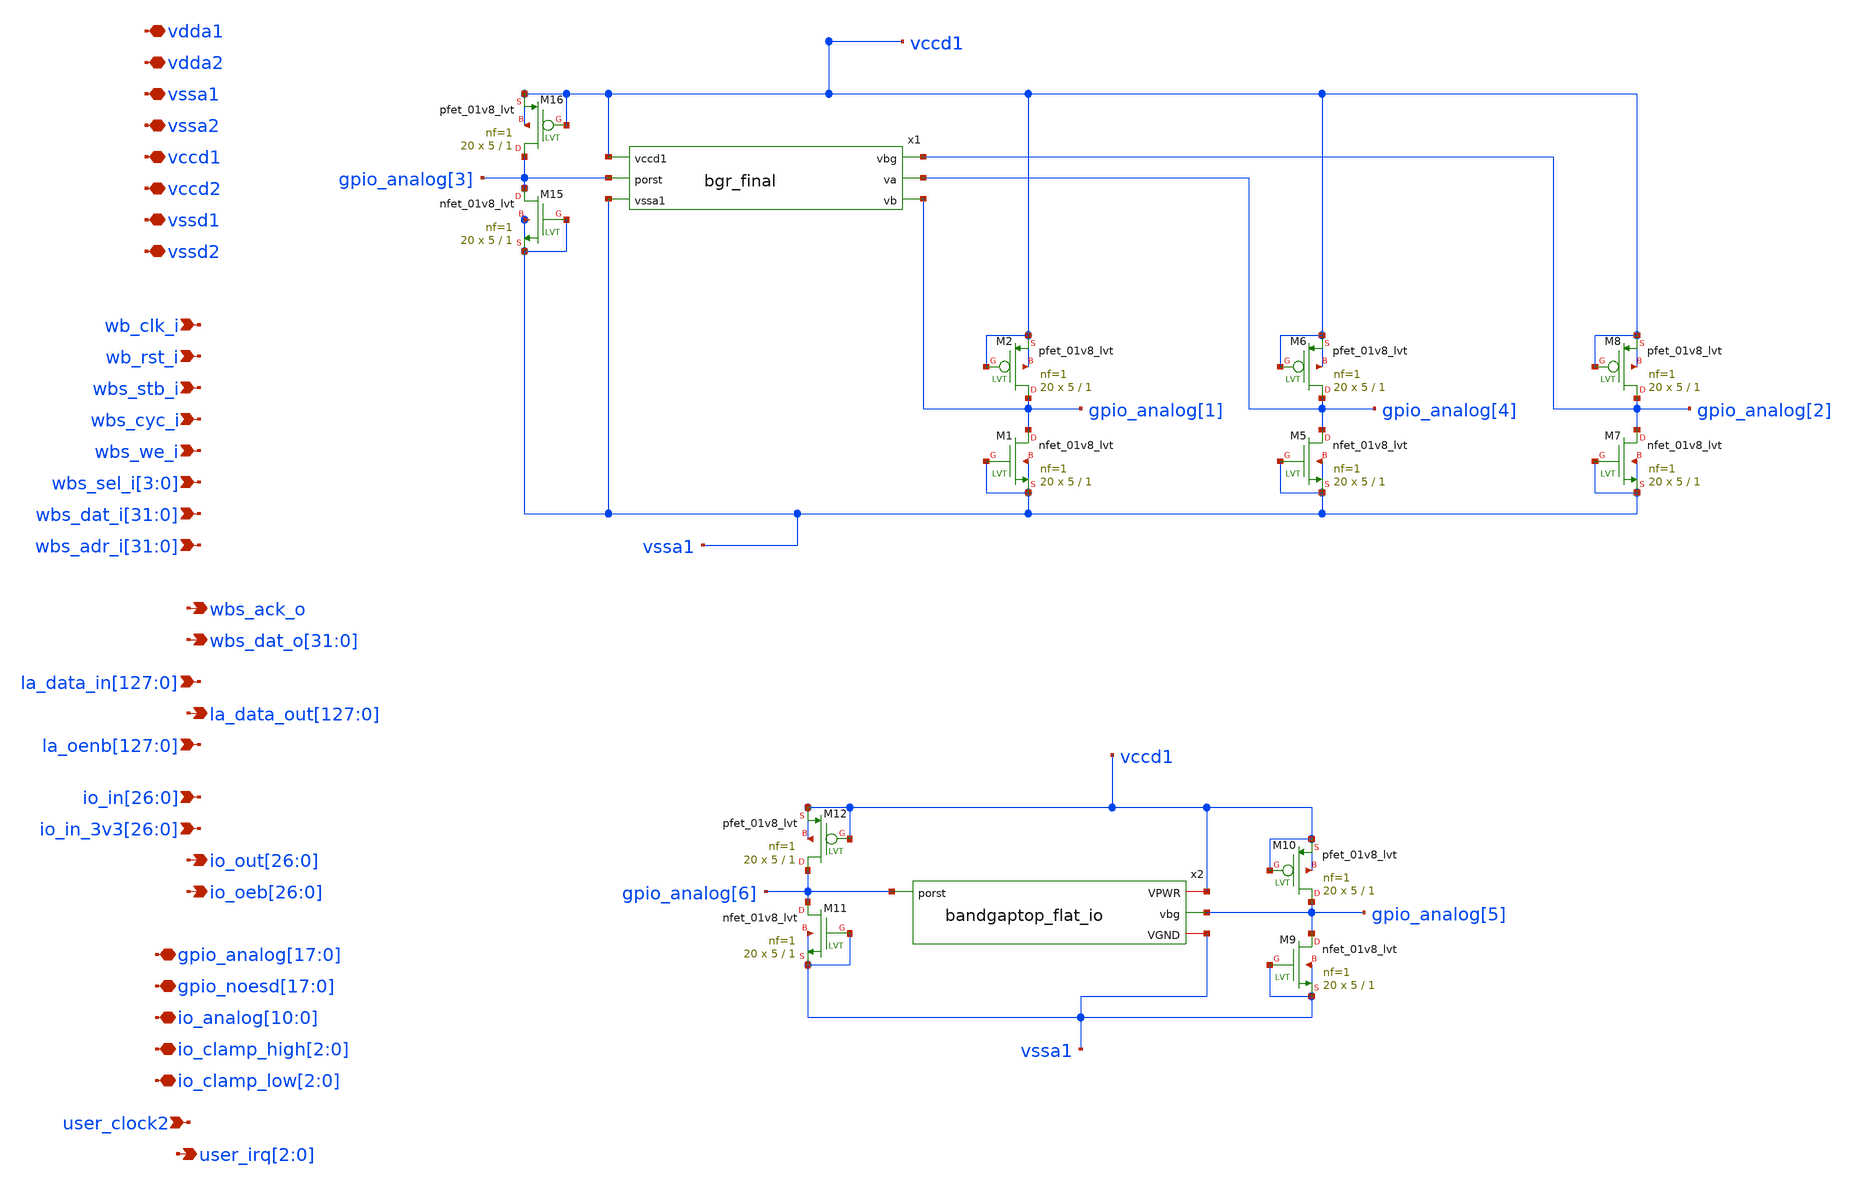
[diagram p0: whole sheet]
** sch_path: xschem/xschem/user_analog_project_wrapper_0.sch
**.subckt user_analog_project_wrapper_0 vdda1 vdda2 vssa1 vssa2 vccd1 vccd2 vssd1 vssd2 wb_clk_i
*+ wb_rst_i wbs_stb_i wbs_cyc_i wbs_we_i wbs_sel_i[3],wbs_sel_i[2],wbs_sel_i[1],wbs_sel_i[0]
*+ wbs_dat_i[31],wbs_dat_i[30],wbs_dat_i[29],wbs_dat_i[28],wbs_dat_i[27],wbs_dat_i[26],wbs_dat_i[25],wbs_dat_i[24],wbs_dat_i[23],wbs_dat_i[22],wbs_dat_i[21],wbs_dat_i[20],wbs_dat_i[19],wbs_dat_i[18],wbs_dat_i[17],wbs_dat_i[16],wbs_dat_i[15],wbs_dat_i[14],wbs_dat_i[13],wbs_dat_i[12],wbs_dat_i[11],wbs_dat_i[10],wbs_dat_i[9],wbs_dat_i[8],wbs_dat_i[7],wbs_dat_i[6],wbs_dat_i[5],wbs_dat_i[4],wbs_dat_i[3],wbs_dat_i[2],wbs_dat_i[1],wbs_dat_i[0]
*+ wbs_adr_i[31],wbs_adr_i[30],wbs_adr_i[29],wbs_adr_i[28],wbs_adr_i[27],wbs_adr_i[26],wbs_adr_i[25],wbs_adr_i[24],wbs_adr_i[23],wbs_adr_i[22],wbs_adr_i[21],wbs_adr_i[20],wbs_adr_i[19],wbs_adr_i[18],wbs_adr_i[17],wbs_adr_i[16],wbs_adr_i[15],wbs_adr_i[14],wbs_adr_i[13],wbs_adr_i[12],wbs_adr_i[11],wbs_adr_i[10],wbs_adr_i[9],wbs_adr_i[8],wbs_adr_i[7],wbs_adr_i[6],wbs_adr_i[5],wbs_adr_i[4],wbs_adr_i[3],wbs_adr_i[2],wbs_adr_i[1],wbs_adr_i[0] wbs_ack_o
*+ wbs_dat_o[31],wbs_dat_o[30],wbs_dat_o[29],wbs_dat_o[28],wbs_dat_o[27],wbs_dat_o[26],wbs_dat_o[25],wbs_dat_o[24],wbs_dat_o[23],wbs_dat_o[22],wbs_dat_o[21],wbs_dat_o[20],wbs_dat_o[19],wbs_dat_o[18],wbs_dat_o[17],wbs_dat_o[16],wbs_dat_o[15],wbs_dat_o[14],wbs_dat_o[13],wbs_dat_o[12],wbs_dat_o[11],wbs_dat_o[10],wbs_dat_o[9],wbs_dat_o[8],wbs_dat_o[7],wbs_dat_o[6],wbs_dat_o[5],wbs_dat_o[4],wbs_dat_o[3],wbs_dat_o[2],wbs_dat_o[1],wbs_dat_o[0]
*+ la_data_in[127],la_data_in[126],la_data_in[125],la_data_in[124],la_data_in[123],la_data_in[122],la_data_in[121],la_data_in[120],la_data_in[119],la_data_in[118],la_data_in[117],la_data_in[116],la_data_in[115],la_data_in[114],la_data_in[113],la_data_in[112],la_data_in[111],la_data_in[110],la_data_in[109],la_data_in[108],la_data_in[107],la_data_in[106],la_data_in[105],la_data_in[104],la_data_in[103],la_data_in[102],la_data_in[101],la_data_in[100],la_data_in[99],la_data_in[98],la_data_in[97],la_data_in[96],la_data_in[95],la_data_in[94],la_data_in[93],la_data_in[92],la_data_in[91],la_data_in[90],la_data_in[89],la_data_in[88],la_data_in[87],la_data_in[86],la_data_in[85],la_data_in[84],la_data_in[83],la_data_in[82],la_data_in[81],la_data_in[80],la_data_in[79],la_data_in[78],la_data_in[77],la_data_in[76],la_data_in[75],la_data_in[74],la_data_in[73],la_data_in[72],la_data_in[71],la_data_in[70],la_data_in[69],la_data_in[68],la_data_in[67],la_data_in[66],la_data_in[65],la_data_in[64],la_data_in[63],la_data_in[62],la_data_in[61],la_data_in[60],la_data_in[59],la_data_in[58],la_data_in[57],la_data_in[56],la_data_in[55],la_data_in[54],la_data_in[53],la_data_in[52],la_data_in[51],la_data_in[50],la_data_in[49],la_data_in[48],la_data_in[47],la_data_in[46],la_data_in[45],la_data_in[44],la_data_in[43],la_data_in[42],la_data_in[41],la_data_in[40],la_data_in[39],la_data_in[38],la_data_in[37],la_data_in[36],la_data_in[35],la_data_in[34],la_data_in[33],la_data_in[32],la_data_in[31],la_data_in[30],la_data_in[29],la_data_in[28],la_data_in[27],la_data_in[26],la_data_in[25],la_data_in[24],la_data_in[23],la_data_in[22],la_data_in[21],la_data_in[20],la_data_in[19],la_data_in[18],la_data_in[17],la_data_in[16],la_data_in[15],la_data_in[14],la_data_in[13],la_data_in[12],la_data_in[11],la_data_in[10],la_data_in[9],la_data_in[8],la_data_in[7],la_data_in[6],la_data_in[5],la_data_in[4],la_data_in[3],la_data_in[2],la_data_in[1],la_data_in[0]
*+ la_data_out[127],la_data_out[126],la_data_out[125],la_data_out[124],la_data_out[123],la_data_out[122],la_data_out[121],la_data_out[120],la_data_out[119],la_data_out[118],la_data_out[117],la_data_out[116],la_data_out[115],la_data_out[114],la_data_out[113],la_data_out[112],la_data_out[111],la_data_out[110],la_data_out[109],la_data_out[108],la_data_out[107],la_data_out[106],la_data_out[105],la_data_out[104],la_data_out[103],la_data_out[102],la_data_out[101],la_data_out[100],la_data_out[99],la_data_out[98],la_data_out[97],la_data_out[96],la_data_out[95],la_data_out[94],la_data_out[93],la_data_out[92],la_data_out[91],la_data_out[90],la_data_out[89],la_data_out[88],la_data_out[87],la_data_out[86],la_data_out[85],la_data_out[84],la_data_out[83],la_data_out[82],la_data_out[81],la_data_out[80],la_data_out[79],la_data_out[78],la_data_out[77],la_data_out[76],la_data_out[75],la_data_out[74],la_data_out[73],la_data_out[72],la_data_out[71],la_data_out[70],la_data_out[69],la_data_out[68],la_data_out[67],la_data_out[66],la_data_out[65],la_data_out[64],la_data_out[63],la_data_out[62],la_data_out[61],la_data_out[60],la_data_out[59],la_data_out[58],la_data_out[57],la_data_out[56],la_data_out[55],la_data_out[54],la_data_out[53],la_data_out[52],la_data_out[51],la_data_out[50],la_data_out[49],la_data_out[48],la_data_out[47],la_data_out[46],la_data_out[45],la_data_out[44],la_data_out[43],la_data_out[42],la_data_out[41],la_data_out[40],la_data_out[39],la_data_out[38],la_data_out[37],la_data_out[36],la_data_out[35],la_data_out[34],la_data_out[33],la_data_out[32],la_data_out[31],la_data_out[30],la_data_out[29],la_data_out[28],la_data_out[27],la_data_out[26],la_data_out[25],la_data_out[24],la_data_out[23],la_data_out[22],la_data_out[21],la_data_out[20],la_data_out[19],la_data_out[18],la_data_out[17],la_data_out[16],la_data_out[15],la_data_out[14],la_data_out[13],la_data_out[12],la_data_out[11],la_data_out[10],la_data_out[9],la_data_out[8],la_data_out[7],la_data_out[6],la_data_out[5],la_data_out[4],la_data_out[3],la_data_out[2],la_data_out[1],la_data_out[0]
*+ io_in[26],io_in[25],io_in[24],io_in[23],io_in[22],io_in[21],io_in[20],io_in[19],io_in[18],io_in[17],io_in[16],io_in[15],io_in[14],io_in[13],io_in[12],io_in[11],io_in[10],io_in[9],io_in[8],io_in[7],io_in[6],io_in[5],io_in[4],io_in[3],io_in[2],io_in[1],io_in[0]
*+ io_in_3v3[26],io_in_3v3[25],io_in_3v3[24],io_in_3v3[23],io_in_3v3[22],io_in_3v3[21],io_in_3v3[20],io_in_3v3[19],io_in_3v3[18],io_in_3v3[17],io_in_3v3[16],io_in_3v3[15],io_in_3v3[14],io_in_3v3[13],io_in_3v3[12],io_in_3v3[11],io_in_3v3[10],io_in_3v3[9],io_in_3v3[8],io_in_3v3[7],io_in_3v3[6],io_in_3v3[5],io_in_3v3[4],io_in_3v3[3],io_in_3v3[2],io_in_3v3[1],io_in_3v3[0] user_clock2
*+ io_out[26],io_out[25],io_out[24],io_out[23],io_out[22],io_out[21],io_out[20],io_out[19],io_out[18],io_out[17],io_out[16],io_out[15],io_out[14],io_out[13],io_out[12],io_out[11],io_out[10],io_out[9],io_out[8],io_out[7],io_out[6],io_out[5],io_out[4],io_out[3],io_out[2],io_out[1],io_out[0]
*+ io_oeb[26],io_oeb[25],io_oeb[24],io_oeb[23],io_oeb[22],io_oeb[21],io_oeb[20],io_oeb[19],io_oeb[18],io_oeb[17],io_oeb[16],io_oeb[15],io_oeb[14],io_oeb[13],io_oeb[12],io_oeb[11],io_oeb[10],io_oeb[9],io_oeb[8],io_oeb[7],io_oeb[6],io_oeb[5],io_oeb[4],io_oeb[3],io_oeb[2],io_oeb[1],io_oeb[0]
*+ gpio_analog[17],gpio_analog[16],gpio_analog[15],gpio_analog[14],gpio_analog[13],gpio_analog[12],gpio_analog[11],gpio_analog[10],gpio_analog[9],gpio_analog[8],gpio_analog[7],gpio_analog[6],gpio_analog[5],gpio_analog[4],gpio_analog[3],gpio_analog[2],gpio_analog[1],gpio_analog[0]
*+ gpio_noesd[17],gpio_noesd[16],gpio_noesd[15],gpio_noesd[14],gpio_noesd[13],gpio_noesd[12],gpio_noesd[11],gpio_noesd[10],gpio_noesd[9],gpio_noesd[8],gpio_noesd[7],gpio_noesd[6],gpio_noesd[5],gpio_noesd[4],gpio_noesd[3],gpio_noesd[2],gpio_noesd[1],gpio_noesd[0]
*+ io_analog[10],io_analog[9],io_analog[8],io_analog[7],io_analog[6],io_analog[5],io_analog[4],io_analog[3],io_analog[2],io_analog[1],io_analog[0] io_clamp_high[2],io_clamp_high[1],io_clamp_high[0] io_clamp_low[2],io_clamp_low[1],io_clamp_low[0]
*+ user_irq[2],user_irq[1],user_irq[0]
*+ la_oenb[127],la_oenb[126],la_oenb[125],la_oenb[124],la_oenb[123],la_oenb[122],la_oenb[121],la_oenb[120],la_oenb[119],la_oenb[118],la_oenb[117],la_oenb[116],la_oenb[115],la_oenb[114],la_oenb[113],la_oenb[112],la_oenb[111],la_oenb[110],la_oenb[109],la_oenb[108],la_oenb[107],la_oenb[106],la_oenb[105],la_oenb[104],la_oenb[103],la_oenb[102],la_oenb[101],la_oenb[100],la_oenb[99],la_oenb[98],la_oenb[97],la_oenb[96],la_oenb[95],la_oenb[94],la_oenb[93],la_oenb[92],la_oenb[91],la_oenb[90],la_oenb[89],la_oenb[88],la_oenb[87],la_oenb[86],la_oenb[85],la_oenb[84],la_oenb[83],la_oenb[82],la_oenb[81],la_oenb[80],la_oenb[79],la_oenb[78],la_oenb[77],la_oenb[76],la_oenb[75],la_oenb[74],la_oenb[73],la_oenb[72],la_oenb[71],la_oenb[70],la_oenb[69],la_oenb[68],la_oenb[67],la_oenb[66],la_oenb[65],la_oenb[64],la_oenb[63],la_oenb[62],la_oenb[61],la_oenb[60],la_oenb[59],la_oenb[58],la_oenb[57],la_oenb[56],la_oenb[55],la_oenb[54],la_oenb[53],la_oenb[52],la_oenb[51],la_oenb[50],la_oenb[49],la_oenb[48],la_oenb[47],la_oenb[46],la_oenb[45],la_oenb[44],la_oenb[43],la_oenb[42],la_oenb[41],la_oenb[40],la_oenb[39],la_oenb[38],la_oenb[37],la_oenb[36],la_oenb[35],la_oenb[34],la_oenb[33],la_oenb[32],la_oenb[31],la_oenb[30],la_oenb[29],la_oenb[28],la_oenb[27],la_oenb[26],la_oenb[25],la_oenb[24],la_oenb[23],la_oenb[22],la_oenb[21],la_oenb[20],la_oenb[19],la_oenb[18],la_oenb[17],la_oenb[16],la_oenb[15],la_oenb[14],la_oenb[13],la_oenb[12],la_oenb[11],la_oenb[10],la_oenb[9],la_oenb[8],la_oenb[7],la_oenb[6],la_oenb[5],la_oenb[4],la_oenb[3],la_oenb[2],la_oenb[1],la_oenb[0]
*.iopin vdda1
*.iopin vdda2
*.iopin vssa1
*.iopin vssa2
*.iopin vccd1
*.iopin vccd2
*.iopin vssd1
*.iopin vssd2
*.ipin wb_clk_i
*.ipin wb_rst_i
*.ipin wbs_stb_i
*.ipin wbs_cyc_i
*.ipin wbs_we_i
*.ipin wbs_sel_i[3],wbs_sel_i[2],wbs_sel_i[1],wbs_sel_i[0]
*.ipin
*+ wbs_dat_i[31],wbs_dat_i[30],wbs_dat_i[29],wbs_dat_i[28],wbs_dat_i[27],wbs_dat_i[26],wbs_dat_i[25],wbs_dat_i[24],wbs_dat_i[23],wbs_dat_i[22],wbs_dat_i[21],wbs_dat_i[20],wbs_dat_i[19],wbs_dat_i[18],wbs_dat_i[17],wbs_dat_i[16],wbs_dat_i[15],wbs_dat_i[14],wbs_dat_i[13],wbs_dat_i[12],wbs_dat_i[11],wbs_dat_i[10],wbs_dat_i[9],wbs_dat_i[8],wbs_dat_i[7],wbs_dat_i[6],wbs_dat_i[5],wbs_dat_i[4],wbs_dat_i[3],wbs_dat_i[2],wbs_dat_i[1],wbs_dat_i[0]
*.ipin
*+ wbs_adr_i[31],wbs_adr_i[30],wbs_adr_i[29],wbs_adr_i[28],wbs_adr_i[27],wbs_adr_i[26],wbs_adr_i[25],wbs_adr_i[24],wbs_adr_i[23],wbs_adr_i[22],wbs_adr_i[21],wbs_adr_i[20],wbs_adr_i[19],wbs_adr_i[18],wbs_adr_i[17],wbs_adr_i[16],wbs_adr_i[15],wbs_adr_i[14],wbs_adr_i[13],wbs_adr_i[12],wbs_adr_i[11],wbs_adr_i[10],wbs_adr_i[9],wbs_adr_i[8],wbs_adr_i[7],wbs_adr_i[6],wbs_adr_i[5],wbs_adr_i[4],wbs_adr_i[3],wbs_adr_i[2],wbs_adr_i[1],wbs_adr_i[0]
*.opin wbs_ack_o
*.opin
*+ wbs_dat_o[31],wbs_dat_o[30],wbs_dat_o[29],wbs_dat_o[28],wbs_dat_o[27],wbs_dat_o[26],wbs_dat_o[25],wbs_dat_o[24],wbs_dat_o[23],wbs_dat_o[22],wbs_dat_o[21],wbs_dat_o[20],wbs_dat_o[19],wbs_dat_o[18],wbs_dat_o[17],wbs_dat_o[16],wbs_dat_o[15],wbs_dat_o[14],wbs_dat_o[13],wbs_dat_o[12],wbs_dat_o[11],wbs_dat_o[10],wbs_dat_o[9],wbs_dat_o[8],wbs_dat_o[7],wbs_dat_o[6],wbs_dat_o[5],wbs_dat_o[4],wbs_dat_o[3],wbs_dat_o[2],wbs_dat_o[1],wbs_dat_o[0]
*.ipin
*+ la_data_in[127],la_data_in[126],la_data_in[125],la_data_in[124],la_data_in[123],la_data_in[122],la_data_in[121],la_data_in[120],la_data_in[119],la_data_in[118],la_data_in[117],la_data_in[116],la_data_in[115],la_data_in[114],la_data_in[113],la_data_in[112],la_data_in[111],la_data_in[110],la_data_in[109],la_data_in[108],la_data_in[107],la_data_in[106],la_data_in[105],la_data_in[104],la_data_in[103],la_data_in[102],la_data_in[101],la_data_in[100],la_data_in[99],la_data_in[98],la_data_in[97],la_data_in[96],la_data_in[95],la_data_in[94],la_data_in[93],la_data_in[92],la_data_in[91],la_data_in[90],la_data_in[89],la_data_in[88],la_data_in[87],la_data_in[86],la_data_in[85],la_data_in[84],la_data_in[83],la_data_in[82],la_data_in[81],la_data_in[80],la_data_in[79],la_data_in[78],la_data_in[77],la_data_in[76],la_data_in[75],la_data_in[74],la_data_in[73],la_data_in[72],la_data_in[71],la_data_in[70],la_data_in[69],la_data_in[68],la_data_in[67],la_data_in[66],la_data_in[65],la_data_in[64],la_data_in[63],la_data_in[62],la_data_in[61],la_data_in[60],la_data_in[59],la_data_in[58],la_data_in[57],la_data_in[56],la_data_in[55],la_data_in[54],la_data_in[53],la_data_in[52],la_data_in[51],la_data_in[50],la_data_in[49],la_data_in[48],la_data_in[47],la_data_in[46],la_data_in[45],la_data_in[44],la_data_in[43],la_data_in[42],la_data_in[41],la_data_in[40],la_data_in[39],la_data_in[38],la_data_in[37],la_data_in[36],la_data_in[35],la_data_in[34],la_data_in[33],la_data_in[32],la_data_in[31],la_data_in[30],la_data_in[29],la_data_in[28],la_data_in[27],la_data_in[26],la_data_in[25],la_data_in[24],la_data_in[23],la_data_in[22],la_data_in[21],la_data_in[20],la_data_in[19],la_data_in[18],la_data_in[17],la_data_in[16],la_data_in[15],la_data_in[14],la_data_in[13],la_data_in[12],la_data_in[11],la_data_in[10],la_data_in[9],la_data_in[8],la_data_in[7],la_data_in[6],la_data_in[5],la_data_in[4],la_data_in[3],la_data_in[2],la_data_in[1],la_data_in[0]
*.opin
*+ la_data_out[127],la_data_out[126],la_data_out[125],la_data_out[124],la_data_out[123],la_data_out[122],la_data_out[121],la_data_out[120],la_data_out[119],la_data_out[118],la_data_out[117],la_data_out[116],la_data_out[115],la_data_out[114],la_data_out[113],la_data_out[112],la_data_out[111],la_data_out[110],la_data_out[109],la_data_out[108],la_data_out[107],la_data_out[106],la_data_out[105],la_data_out[104],la_data_out[103],la_data_out[102],la_data_out[101],la_data_out[100],la_data_out[99],la_data_out[98],la_data_out[97],la_data_out[96],la_data_out[95],la_data_out[94],la_data_out[93],la_data_out[92],la_data_out[91],la_data_out[90],la_data_out[89],la_data_out[88],la_data_out[87],la_data_out[86],la_data_out[85],la_data_out[84],la_data_out[83],la_data_out[82],la_data_out[81],la_data_out[80],la_data_out[79],la_data_out[78],la_data_out[77],la_data_out[76],la_data_out[75],la_data_out[74],la_data_out[73],la_data_out[72],la_data_out[71],la_data_out[70],la_data_out[69],la_data_out[68],la_data_out[67],la_data_out[66],la_data_out[65],la_data_out[64],la_data_out[63],la_data_out[62],la_data_out[61],la_data_out[60],la_data_out[59],la_data_out[58],la_data_out[57],la_data_out[56],la_data_out[55],la_data_out[54],la_data_out[53],la_data_out[52],la_data_out[51],la_data_out[50],la_data_out[49],la_data_out[48],la_data_out[47],la_data_out[46],la_data_out[45],la_data_out[44],la_data_out[43],la_data_out[42],la_data_out[41],la_data_out[40],la_data_out[39],la_data_out[38],la_data_out[37],la_data_out[36],la_data_out[35],la_data_out[34],la_data_out[33],la_data_out[32],la_data_out[31],la_data_out[30],la_data_out[29],la_data_out[28],la_data_out[27],la_data_out[26],la_data_out[25],la_data_out[24],la_data_out[23],la_data_out[22],la_data_out[21],la_data_out[20],la_data_out[19],la_data_out[18],la_data_out[17],la_data_out[16],la_data_out[15],la_data_out[14],la_data_out[13],la_data_out[12],la_data_out[11],la_data_out[10],la_data_out[9],la_data_out[8],la_data_out[7],la_data_out[6],la_data_out[5],la_data_out[4],la_data_out[3],la_data_out[2],la_data_out[1],la_data_out[0]
*.ipin
*+ io_in[26],io_in[25],io_in[24],io_in[23],io_in[22],io_in[21],io_in[20],io_in[19],io_in[18],io_in[17],io_in[16],io_in[15],io_in[14],io_in[13],io_in[12],io_in[11],io_in[10],io_in[9],io_in[8],io_in[7],io_in[6],io_in[5],io_in[4],io_in[3],io_in[2],io_in[1],io_in[0]
*.ipin
*+ io_in_3v3[26],io_in_3v3[25],io_in_3v3[24],io_in_3v3[23],io_in_3v3[22],io_in_3v3[21],io_in_3v3[20],io_in_3v3[19],io_in_3v3[18],io_in_3v3[17],io_in_3v3[16],io_in_3v3[15],io_in_3v3[14],io_in_3v3[13],io_in_3v3[12],io_in_3v3[11],io_in_3v3[10],io_in_3v3[9],io_in_3v3[8],io_in_3v3[7],io_in_3v3[6],io_in_3v3[5],io_in_3v3[4],io_in_3v3[3],io_in_3v3[2],io_in_3v3[1],io_in_3v3[0]
*.ipin user_clock2
*.opin
*+ io_out[26],io_out[25],io_out[24],io_out[23],io_out[22],io_out[21],io_out[20],io_out[19],io_out[18],io_out[17],io_out[16],io_out[15],io_out[14],io_out[13],io_out[12],io_out[11],io_out[10],io_out[9],io_out[8],io_out[7],io_out[6],io_out[5],io_out[4],io_out[3],io_out[2],io_out[1],io_out[0]
*.opin
*+ io_oeb[26],io_oeb[25],io_oeb[24],io_oeb[23],io_oeb[22],io_oeb[21],io_oeb[20],io_oeb[19],io_oeb[18],io_oeb[17],io_oeb[16],io_oeb[15],io_oeb[14],io_oeb[13],io_oeb[12],io_oeb[11],io_oeb[10],io_oeb[9],io_oeb[8],io_oeb[7],io_oeb[6],io_oeb[5],io_oeb[4],io_oeb[3],io_oeb[2],io_oeb[1],io_oeb[0]
*.iopin
*+ gpio_analog[17],gpio_analog[16],gpio_analog[15],gpio_analog[14],gpio_analog[13],gpio_analog[12],gpio_analog[11],gpio_analog[10],gpio_analog[9],gpio_analog[8],gpio_analog[7],gpio_analog[6],gpio_analog[5],gpio_analog[4],gpio_analog[3],gpio_analog[2],gpio_analog[1],gpio_analog[0]
*.iopin
*+ gpio_noesd[17],gpio_noesd[16],gpio_noesd[15],gpio_noesd[14],gpio_noesd[13],gpio_noesd[12],gpio_noesd[11],gpio_noesd[10],gpio_noesd[9],gpio_noesd[8],gpio_noesd[7],gpio_noesd[6],gpio_noesd[5],gpio_noesd[4],gpio_noesd[3],gpio_noesd[2],gpio_noesd[1],gpio_noesd[0]
*.iopin
*+ io_analog[10],io_analog[9],io_analog[8],io_analog[7],io_analog[6],io_analog[5],io_analog[4],io_analog[3],io_analog[2],io_analog[1],io_analog[0]
*.iopin io_clamp_high[2],io_clamp_high[1],io_clamp_high[0]
*.iopin io_clamp_low[2],io_clamp_low[1],io_clamp_low[0]
*.opin user_irq[2],user_irq[1],user_irq[0]
*.ipin
*+ la_oenb[127],la_oenb[126],la_oenb[125],la_oenb[124],la_oenb[123],la_oenb[122],la_oenb[121],la_oenb[120],la_oenb[119],la_oenb[118],la_oenb[117],la_oenb[116],la_oenb[115],la_oenb[114],la_oenb[113],la_oenb[112],la_oenb[111],la_oenb[110],la_oenb[109],la_oenb[108],la_oenb[107],la_oenb[106],la_oenb[105],la_oenb[104],la_oenb[103],la_oenb[102],la_oenb[101],la_oenb[100],la_oenb[99],la_oenb[98],la_oenb[97],la_oenb[96],la_oenb[95],la_oenb[94],la_oenb[93],la_oenb[92],la_oenb[91],la_oenb[90],la_oenb[89],la_oenb[88],la_oenb[87],la_oenb[86],la_oenb[85],la_oenb[84],la_oenb[83],la_oenb[82],la_oenb[81],la_oenb[80],la_oenb[79],la_oenb[78],la_oenb[77],la_oenb[76],la_oenb[75],la_oenb[74],la_oenb[73],la_oenb[72],la_oenb[71],la_oenb[70],la_oenb[69],la_oenb[68],la_oenb[67],la_oenb[66],la_oenb[65],la_oenb[64],la_oenb[63],la_oenb[62],la_oenb[61],la_oenb[60],la_oenb[59],la_oenb[58],la_oenb[57],la_oenb[56],la_oenb[55],la_oenb[54],la_oenb[53],la_oenb[52],la_oenb[51],la_oenb[50],la_oenb[49],la_oenb[48],la_oenb[47],la_oenb[46],la_oenb[45],la_oenb[44],la_oenb[43],la_oenb[42],la_oenb[41],la_oenb[40],la_oenb[39],la_oenb[38],la_oenb[37],la_oenb[36],la_oenb[35],la_oenb[34],la_oenb[33],la_oenb[32],la_oenb[31],la_oenb[30],la_oenb[29],la_oenb[28],la_oenb[27],la_oenb[26],la_oenb[25],la_oenb[24],la_oenb[23],la_oenb[22],la_oenb[21],la_oenb[20],la_oenb[19],la_oenb[18],la_oenb[17],la_oenb[16],la_oenb[15],la_oenb[14],la_oenb[13],la_oenb[12],la_oenb[11],la_oenb[10],la_oenb[9],la_oenb[8],la_oenb[7],la_oenb[6],la_oenb[5],la_oenb[4],la_oenb[3],la_oenb[2],la_oenb[1],la_oenb[0]
XM1 gpio_analog[1] vssa1 vssa1 vssa1 sky130_fd_pr__nfet_01v8_lvt L=1 W=5 nf=1 ad='int((nf+1)/2) * W/nf * 0.29'
+ as='int((nf+2)/2) * W/nf * 0.29' pd='2*int((nf+1)/2) * (W/nf + 0.29)' ps='2*int((nf+2)/2) * (W/nf + 0.29)'
+ nrd='0.29 / W' nrs='0.29 / W' sa=0 sb=0 sd=0 mult=20 m=20
XM2 gpio_analog[1] vccd1 vccd1 vccd1 sky130_fd_pr__pfet_01v8_lvt L=1 W=5 nf=1 ad='int((nf+1)/2) * W/nf * 0.29'
+ as='int((nf+2)/2) * W/nf * 0.29' pd='2*int((nf+1)/2) * (W/nf + 0.29)' ps='2*int((nf+2)/2) * (W/nf + 0.29)'
+ nrd='0.29 / W' nrs='0.29 / W' sa=0 sb=0 sd=0 mult=20 m=20
XM5 gpio_analog[4] vssa1 vssa1 vssa1 sky130_fd_pr__nfet_01v8_lvt L=1 W=5 nf=1 ad='int((nf+1)/2) * W/nf * 0.29'
+ as='int((nf+2)/2) * W/nf * 0.29' pd='2*int((nf+1)/2) * (W/nf + 0.29)' ps='2*int((nf+2)/2) * (W/nf + 0.29)'
+ nrd='0.29 / W' nrs='0.29 / W' sa=0 sb=0 sd=0 mult=20 m=20
XM6 gpio_analog[4] vccd1 vccd1 vccd1 sky130_fd_pr__pfet_01v8_lvt L=1 W=5 nf=1 ad='int((nf+1)/2) * W/nf * 0.29'
+ as='int((nf+2)/2) * W/nf * 0.29' pd='2*int((nf+1)/2) * (W/nf + 0.29)' ps='2*int((nf+2)/2) * (W/nf + 0.29)'
+ nrd='0.29 / W' nrs='0.29 / W' sa=0 sb=0 sd=0 mult=20 m=20
XM7 gpio_analog[2] vssa1 vssa1 vssa1 sky130_fd_pr__nfet_01v8_lvt L=1 W=5 nf=1 ad='int((nf+1)/2) * W/nf * 0.29'
+ as='int((nf+2)/2) * W/nf * 0.29' pd='2*int((nf+1)/2) * (W/nf + 0.29)' ps='2*int((nf+2)/2) * (W/nf + 0.29)'
+ nrd='0.29 / W' nrs='0.29 / W' sa=0 sb=0 sd=0 mult=20 m=20
XM8 gpio_analog[2] vccd1 vccd1 vccd1 sky130_fd_pr__pfet_01v8_lvt L=1 W=5 nf=1 ad='int((nf+1)/2) * W/nf * 0.29'
+ as='int((nf+2)/2) * W/nf * 0.29' pd='2*int((nf+1)/2) * (W/nf + 0.29)' ps='2*int((nf+2)/2) * (W/nf + 0.29)'
+ nrd='0.29 / W' nrs='0.29 / W' sa=0 sb=0 sd=0 mult=20 m=20
x1 vccd1 gpio_analog[3] gpio_analog[2] gpio_analog[4] gpio_analog[1] vssa1 bgr_final
XM9 gpio_analog[5] vssa1 vssa1 vssa1 sky130_fd_pr__nfet_01v8_lvt L=1 W=5 nf=1 ad='int((nf+1)/2) * W/nf * 0.29'
+ as='int((nf+2)/2) * W/nf * 0.29' pd='2*int((nf+1)/2) * (W/nf + 0.29)' ps='2*int((nf+2)/2) * (W/nf + 0.29)'
+ nrd='0.29 / W' nrs='0.29 / W' sa=0 sb=0 sd=0 mult=20 m=20
XM10 gpio_analog[5] vccd1 vccd1 vccd1 sky130_fd_pr__pfet_01v8_lvt L=1 W=5 nf=1 ad='int((nf+1)/2) * W/nf * 0.29'
+ as='int((nf+2)/2) * W/nf * 0.29' pd='2*int((nf+1)/2) * (W/nf + 0.29)' ps='2*int((nf+2)/2) * (W/nf + 0.29)'
+ nrd='0.29 / W' nrs='0.29 / W' sa=0 sb=0 sd=0 mult=20 m=20
XM11 gpio_analog[6] vssa1 vssa1 vssa1 sky130_fd_pr__nfet_01v8_lvt L=1 W=5 nf=1 ad='int((nf+1)/2) * W/nf * 0.29'
+ as='int((nf+2)/2) * W/nf * 0.29' pd='2*int((nf+1)/2) * (W/nf + 0.29)' ps='2*int((nf+2)/2) * (W/nf + 0.29)'
+ nrd='0.29 / W' nrs='0.29 / W' sa=0 sb=0 sd=0 mult=20 m=20
XM12 gpio_analog[6] vccd1 vccd1 vccd1 sky130_fd_pr__pfet_01v8_lvt L=1 W=5 nf=1 ad='int((nf+1)/2) * W/nf * 0.29'
+ as='int((nf+2)/2) * W/nf * 0.29' pd='2*int((nf+1)/2) * (W/nf + 0.29)' ps='2*int((nf+2)/2) * (W/nf + 0.29)'
+ nrd='0.29 / W' nrs='0.29 / W' sa=0 sb=0 sd=0 mult=20 m=20
XM15 gpio_analog[3] vssa1 vssa1 vssa1 sky130_fd_pr__nfet_01v8_lvt L=1 W=5 nf=1 ad='int((nf+1)/2) * W/nf * 0.29'
+ as='int((nf+2)/2) * W/nf * 0.29' pd='2*int((nf+1)/2) * (W/nf + 0.29)' ps='2*int((nf+2)/2) * (W/nf + 0.29)'
+ nrd='0.29 / W' nrs='0.29 / W' sa=0 sb=0 sd=0 mult=20 m=20
XM16 gpio_analog[3] vccd1 vccd1 vccd1 sky130_fd_pr__pfet_01v8_lvt L=1 W=5 nf=1 ad='int((nf+1)/2) * W/nf * 0.29'
+ as='int((nf+2)/2) * W/nf * 0.29' pd='2*int((nf+1)/2) * (W/nf + 0.29)' ps='2*int((nf+2)/2) * (W/nf + 0.29)'
+ nrd='0.29 / W' nrs='0.29 / W' sa=0 sb=0 sd=0 mult=20 m=20
x2 vccd1 gpio_analog[6] gpio_analog[5] vssa1 bandgaptop_flat_io
**.ends

* expanding   symbol:  bgr_final.sym # of pins=6
** sym_path: xschem/xschem/bgr_final.sym
** sch_path: xschem/xschem/bgr_final.sch
.subckt bgr_final vccd1 porst vbg va vb vssa1
*.ipin porst
*.opin vbg
*.opin va
*.opin vb
*.ipin vccd1
*.ipin vssa1
XM5 vgate va vq vssa1 sky130_fd_pr__nfet_01v8_lvt L=2 W=4 nf=1 ad='int((nf+1)/2) * W/nf * 0.29' as='int((nf+2)/2) * W/nf * 0.29'
+ pd='2*int((nf+1)/2) * (W/nf + 0.29)' ps='2*int((nf+2)/2) * (W/nf + 0.29)' nrd='0.29 / W' nrs='0.29 / W'
+ sa=0 sb=0 sd=0 mult=9 m=9
XM6 vq Vx vssa1 vssa1 sky130_fd_pr__nfet_01v8_lvt L=2 W=4 nf=1 ad='int((nf+1)/2) * W/nf * 0.29' as='int((nf+2)/2) * W/nf * 0.29'
+ pd='2*int((nf+1)/2) * (W/nf + 0.29)' ps='2*int((nf+2)/2) * (W/nf + 0.29)' nrd='0.29 / W' nrs='0.29 / W'
+ sa=0 sb=0 sd=0 mult=1 m=1
XM9 vg vb vq vssa1 sky130_fd_pr__nfet_01v8_lvt L=2 W=4 nf=1 ad='int((nf+1)/2) * W/nf * 0.29' as='int((nf+2)/2) * W/nf * 0.29'
+ pd='2*int((nf+1)/2) * (W/nf + 0.29)' ps='2*int((nf+2)/2) * (W/nf + 0.29)' nrd='0.29 / W' nrs='0.29 / W'
+ sa=0 sb=0 sd=0 mult=9 m=9
XM7 Vx Vx vssa1 vssa1 sky130_fd_pr__nfet_01v8_lvt L=2 W=4 nf=1 ad='int((nf+1)/2) * W/nf * 0.29' as='int((nf+2)/2) * W/nf * 0.29'
+ pd='2*int((nf+1)/2) * (W/nf + 0.29)' ps='2*int((nf+2)/2) * (W/nf + 0.29)' nrd='0.29 / W' nrs='0.29 / W'
+ sa=0 sb=0 sd=0 mult=1 m=1
XM13 Vx vgate vccd1 vccd1 sky130_fd_pr__pfet_01v8_lvt L=2 W=6.45 nf=1 ad='int((nf+1)/2) * W/nf * 0.29'
+ as='int((nf+2)/2) * W/nf * 0.29' pd='2*int((nf+1)/2) * (W/nf + 0.29)' ps='2*int((nf+2)/2) * (W/nf + 0.29)'
+ nrd='0.29 / W' nrs='0.29 / W' sa=0 sb=0 sd=0 mult=12 m=12
XM1 va vgate vccd1 vccd1 sky130_fd_pr__pfet_01v8_lvt L=2 W=6.45 nf=1 ad='int((nf+1)/2) * W/nf * 0.29'
+ as='int((nf+2)/2) * W/nf * 0.29' pd='2*int((nf+1)/2) * (W/nf + 0.29)' ps='2*int((nf+2)/2) * (W/nf + 0.29)'
+ nrd='0.29 / W' nrs='0.29 / W' sa=0 sb=0 sd=0 mult=60 m=60
XM2 vb vgate vccd1 vccd1 sky130_fd_pr__pfet_01v8_lvt L=2 W=6.45 nf=1 ad='int((nf+1)/2) * W/nf * 0.29'
+ as='int((nf+2)/2) * W/nf * 0.29' pd='2*int((nf+1)/2) * (W/nf + 0.29)' ps='2*int((nf+2)/2) * (W/nf + 0.29)'
+ nrd='0.29 / W' nrs='0.29 / W' sa=0 sb=0 sd=0 mult=60 m=60
XM3 vbg vgate vccd1 vccd1 sky130_fd_pr__pfet_01v8_lvt L=2 W=6.45 nf=1 ad='int((nf+1)/2) * W/nf * 0.29'
+ as='int((nf+2)/2) * W/nf * 0.29' pd='2*int((nf+1)/2) * (W/nf + 0.29)' ps='2*int((nf+2)/2) * (W/nf + 0.29)'
+ nrd='0.29 / W' nrs='0.29 / W' sa=0 sb=0 sd=0 mult=60 m=60
XM4 vg vg vccd1 vccd1 sky130_fd_pr__pfet_01v8_lvt L=2 W=6.45 nf=1 ad='int((nf+1)/2) * W/nf * 0.29' as='int((nf+2)/2) * W/nf * 0.29'
+ pd='2*int((nf+1)/2) * (W/nf + 0.29)' ps='2*int((nf+2)/2) * (W/nf + 0.29)' nrd='0.29 / W' nrs='0.29 / W'
+ sa=0 sb=0 sd=0 mult=6 m=6
XM8 vgate vg vccd1 vccd1 sky130_fd_pr__pfet_01v8_lvt L=2 W=6.45 nf=1 ad='int((nf+1)/2) * W/nf * 0.29'
+ as='int((nf+2)/2) * W/nf * 0.29' pd='2*int((nf+1)/2) * (W/nf + 0.29)' ps='2*int((nf+2)/2) * (W/nf + 0.29)'
+ nrd='0.29 / W' nrs='0.29 / W' sa=0 sb=0 sd=0 mult=6 m=6
XM10 vgate porst vssa1 vssa1 sky130_fd_pr__nfet_01v8_lvt L='2' W='4' nf=1 ad='int((nf+1)/2) * W/nf * 0.29'
+ as='int((nf+2)/2) * W/nf * 0.29' pd='2*int((nf+1)/2) * (W/nf + 0.29)' ps='2*int((nf+2)/2) * (W/nf + 0.29)'
+ nrd='0.29 / W' nrs='0.29 / W' sa=0 sb=0 sd=0 mult=9 m=9
XM17 va vccd1 vccd1 vccd1 sky130_fd_pr__pfet_01v8_lvt L=2 W=6.45 nf=1 ad='int((nf+1)/2) * W/nf * 0.29'
+ as='int((nf+2)/2) * W/nf * 0.29' pd='2*int((nf+1)/2) * (W/nf + 0.29)' ps='2*int((nf+2)/2) * (W/nf + 0.29)'
+ nrd='0.29 / W' nrs='0.29 / W' sa=0 sb=0 sd=0 mult=12 m=12
XC1 vgate vccd1 sky130_fd_pr__cap_mim_m3_1 W=2 L=2 MF=100 m=100
XC2 vssa1 va sky130_fd_pr__cap_mim_m3_1 W=2 L=2 MF=100 m=100
x1 net6 net5 vccd1 vssa1 vssa1 skywater_asc_res_xhigh_po_2p85_1
x2 net7 net6 vccd1 vssa1 vssa1 skywater_asc_res_xhigh_po_2p85_1
x3 net8 net7 vccd1 vssa1 vssa1 skywater_asc_res_xhigh_po_2p85_1
x4 net9 net8 vccd1 vssa1 vssa1 skywater_asc_res_xhigh_po_2p85_1
x5 net5 va vccd1 vssa1 vssa1 skywater_asc_res_xhigh_po_2p85_1
x6 net11 net10 vccd1 vssa1 vssa1 skywater_asc_res_xhigh_po_2p85_1
x13 net4 net11 vccd1 vssa1 vssa1 skywater_asc_res_xhigh_po_2p85_1
x14 net3 net4 vccd1 vssa1 vssa1 skywater_asc_res_xhigh_po_2p85_1
x15 net2 net3 vccd1 vssa1 vssa1 skywater_asc_res_xhigh_po_2p85_1
x16 net10 net9 vccd1 vssa1 vssa1 skywater_asc_res_xhigh_po_2p85_1
x32 net25 net24 vccd1 vssa1 vssa1 skywater_asc_res_xhigh_po_2p85_1
x33 net26 net25 vccd1 vssa1 vssa1 skywater_asc_res_xhigh_po_2p85_1
x34 net27 net26 vccd1 vssa1 vssa1 skywater_asc_res_xhigh_po_2p85_1
x35 net28 net27 vccd1 vssa1 vssa1 skywater_asc_res_xhigh_po_2p85_1
x36 net24 vbg vccd1 vssa1 vssa1 skywater_asc_res_xhigh_po_2p85_1
x37 net22 net29 vccd1 vssa1 vssa1 skywater_asc_res_xhigh_po_2p85_1
x38 net23 net22 vccd1 vssa1 vssa1 skywater_asc_res_xhigh_po_2p85_1
x39 vssa1 net23 vccd1 vssa1 vssa1 skywater_asc_res_xhigh_po_2p85_1
x41 net29 net28 vccd1 vssa1 vssa1 skywater_asc_res_xhigh_po_2p85_1
x23 net1 vb vccd1 vssa1 vssa1 skywater_asc_res_xhigh_po_2p85_1
x24 vbneg net1 vccd1 vssa1 vssa1 skywater_asc_res_xhigh_po_2p85_1
x17 vssa1 net2 vccd1 vssa1 vssa1 skywater_asc_res_xhigh_po_2p85_2
x31 vccd1 vssa1 vssa1 vssa1 vbneg vssa1 sky130_asc_pnp_05v5_W3p40L3p40_8
x26 vccd1 vssa1 vssa1 vssa1 vbneg vssa1 sky130_asc_pnp_05v5_W3p40L3p40_8
x27 vccd1 vssa1 vssa1 vssa1 vbneg vssa1 sky130_asc_pnp_05v5_W3p40L3p40_8
x28 vccd1 vssa1 vssa1 vssa1 vbneg vssa1 sky130_asc_pnp_05v5_W3p40L3p40_8
x29 vccd1 vssa1 vssa1 vssa1 vbneg vssa1 sky130_asc_pnp_05v5_W3p40L3p40_7
x25 net30 vssa1 net31 net32 net33 sky130_asc_pnp_05v5_W3p40L3p40_1
x7 net16 net15 vccd1 vssa1 vssa1 skywater_asc_res_xhigh_po_2p85_1
x8 net17 net16 vccd1 vssa1 vssa1 skywater_asc_res_xhigh_po_2p85_1
x9 net18 net17 vccd1 vssa1 vssa1 skywater_asc_res_xhigh_po_2p85_1
x10 net19 net18 vccd1 vssa1 vssa1 skywater_asc_res_xhigh_po_2p85_1
x11 net15 vb vccd1 vssa1 vssa1 skywater_asc_res_xhigh_po_2p85_1
x12 net21 net20 vccd1 vssa1 vssa1 skywater_asc_res_xhigh_po_2p85_1
x18 net14 net21 vccd1 vssa1 vssa1 skywater_asc_res_xhigh_po_2p85_1
x19 net13 net14 vccd1 vssa1 vssa1 skywater_asc_res_xhigh_po_2p85_1
x20 net12 net13 vccd1 vssa1 vssa1 skywater_asc_res_xhigh_po_2p85_1
x21 net20 net19 vccd1 vssa1 vssa1 skywater_asc_res_xhigh_po_2p85_1
x22 vssa1 net12 vccd1 vssa1 vssa1 skywater_asc_res_xhigh_po_2p85_2
.ends


* expanding   symbol:  xschem/bandgaptop_flat_io.sym # of pins=4
** sym_path: xschem/xschem/bandgaptop_flat_io.sym
** sch_path: xschem/xschem/bandgaptop_flat_io.sch
.subckt bandgaptop_flat_io VPWR porst vbg VGND
*.ipin porst
*.opin vbg
*.iopin VGND
*.iopin VPWR
XM5 vgate Va Vq VGND sky130_fd_pr__nfet_01v8_lvt L=2 W=9 nf=1 ad='int((nf+1)/2) * W/nf * 0.29' as='int((nf+2)/2) * W/nf * 0.29'
+ pd='2*int((nf+1)/2) * (W/nf + 0.29)' ps='2*int((nf+2)/2) * (W/nf + 0.29)' nrd='0.29 / W' nrs='0.29 / W'
+ sa=0 sb=0 sd=0 mult=3 m=3
XM6 Vq Vx VGND VGND sky130_fd_pr__nfet_01v8_lvt L=2 W=2 nf=1 ad='int((nf+1)/2) * W/nf * 0.29' as='int((nf+2)/2) * W/nf * 0.29'
+ pd='2*int((nf+1)/2) * (W/nf + 0.29)' ps='2*int((nf+2)/2) * (W/nf + 0.29)' nrd='0.29 / W' nrs='0.29 / W'
+ sa=0 sb=0 sd=0 mult=2 m=2
XM9 vg Vb Vq VGND sky130_fd_pr__nfet_01v8_lvt L=2 W=9 nf=1 ad='int((nf+1)/2) * W/nf * 0.29' as='int((nf+2)/2) * W/nf * 0.29'
+ pd='2*int((nf+1)/2) * (W/nf + 0.29)' ps='2*int((nf+2)/2) * (W/nf + 0.29)' nrd='0.29 / W' nrs='0.29 / W'
+ sa=0 sb=0 sd=0 mult=3 m=3
XM7 Vx Vx VGND VGND sky130_fd_pr__nfet_01v8_lvt L=2 W=2 nf=1 ad='int((nf+1)/2) * W/nf * 0.29' as='int((nf+2)/2) * W/nf * 0.29'
+ pd='2*int((nf+1)/2) * (W/nf + 0.29)' ps='2*int((nf+2)/2) * (W/nf + 0.29)' nrd='0.29 / W' nrs='0.29 / W'
+ sa=0 sb=0 sd=0 mult=2 m=2
XM13 Vx vgate VPWR VPWR sky130_fd_pr__pfet_01v8_lvt L=2 W=12.9 nf=1 ad='int((nf+1)/2) * W/nf * 0.29'
+ as='int((nf+2)/2) * W/nf * 0.29' pd='2*int((nf+1)/2) * (W/nf + 0.29)' ps='2*int((nf+2)/2) * (W/nf + 0.29)'
+ nrd='0.29 / W' nrs='0.29 / W' sa=0 sb=0 sd=0 mult=6 m=6
XM1 Va vgate VPWR VPWR sky130_fd_pr__pfet_01v8_lvt L=2 W=38.7 nf=1 ad='int((nf+1)/2) * W/nf * 0.29' as='int((nf+2)/2) * W/nf * 0.29'
+ pd='2*int((nf+1)/2) * (W/nf + 0.29)' ps='2*int((nf+2)/2) * (W/nf + 0.29)' nrd='0.29 / W' nrs='0.29 / W'
+ sa=0 sb=0 sd=0 mult=10 m=10
XM2 Vb vgate VPWR VPWR sky130_fd_pr__pfet_01v8_lvt L=2 W=38.7 nf=1 ad='int((nf+1)/2) * W/nf * 0.29' as='int((nf+2)/2) * W/nf * 0.29'
+ pd='2*int((nf+1)/2) * (W/nf + 0.29)' ps='2*int((nf+2)/2) * (W/nf + 0.29)' nrd='0.29 / W' nrs='0.29 / W'
+ sa=0 sb=0 sd=0 mult=10 m=10
XM3 vbg vgate VPWR VPWR sky130_fd_pr__pfet_01v8_lvt L=2 W=38.7 nf=1 ad='int((nf+1)/2) * W/nf * 0.29'
+ as='int((nf+2)/2) * W/nf * 0.29' pd='2*int((nf+1)/2) * (W/nf + 0.29)' ps='2*int((nf+2)/2) * (W/nf + 0.29)'
+ nrd='0.29 / W' nrs='0.29 / W' sa=0 sb=0 sd=0 mult=10 m=10
XM4 vg vg VPWR VPWR sky130_fd_pr__pfet_01v8_lvt L=2 W=12.9 nf=1 ad='int((nf+1)/2) * W/nf * 0.29' as='int((nf+2)/2) * W/nf * 0.29'
+ pd='2*int((nf+1)/2) * (W/nf + 0.29)' ps='2*int((nf+2)/2) * (W/nf + 0.29)' nrd='0.29 / W' nrs='0.29 / W'
+ sa=0 sb=0 sd=0 mult=3 m=3
XM8 vgate vg VPWR VPWR sky130_fd_pr__pfet_01v8_lvt L=2 W=12.9 nf=1 ad='int((nf+1)/2) * W/nf * 0.29' as='int((nf+2)/2) * W/nf * 0.29'
+ pd='2*int((nf+1)/2) * (W/nf + 0.29)' ps='2*int((nf+2)/2) * (W/nf + 0.29)' nrd='0.29 / W' nrs='0.29 / W'
+ sa=0 sb=0 sd=0 mult=3 m=3
XM10 vgate porst VGND VGND sky130_fd_pr__nfet_01v8_lvt L='2' W='1' nf=1 ad='int((nf+1)/2) * W/nf * 0.29'
+ as='int((nf+2)/2) * W/nf * 0.29' pd='2*int((nf+1)/2) * (W/nf + 0.29)' ps='2*int((nf+2)/2) * (W/nf + 0.29)'
+ nrd='0.29 / W' nrs='0.29 / W' sa=0 sb=0 sd=0 mult=27 m=27
XR6 net1 Va VGND sky130_fd_pr__res_xhigh_po_2p85 L=31.52 mult=1 m=1
XR7 net2 net1 VGND sky130_fd_pr__res_xhigh_po_2p85 L=31.52 mult=1 m=1
XR8 net3 net2 VGND sky130_fd_pr__res_xhigh_po_2p85 L=31.52 mult=1 m=1
XR10 net4 net3 VGND sky130_fd_pr__res_xhigh_po_2p85 L=31.52 mult=1 m=1
XR11 net5 net4 VGND sky130_fd_pr__res_xhigh_po_2p85 L=31.52 mult=1 m=1
XR9 VGND net5 VGND sky130_fd_pr__res_xhigh_po_2p85 L=21.5 mult=1 m=1
XR3 vdm Vb VGND sky130_fd_pr__res_xhigh_po_2p85 L=31.52 mult=1 m=1
XR1 net6 Vb VGND sky130_fd_pr__res_xhigh_po_2p85 L=31.52 mult=1 m=1
XR2 net7 net6 VGND sky130_fd_pr__res_xhigh_po_2p85 L=31.52 mult=1 m=1
XR4 net8 net7 VGND sky130_fd_pr__res_xhigh_po_2p85 L=31.52 mult=1 m=1
XR5 net9 net8 VGND sky130_fd_pr__res_xhigh_po_2p85 L=31.52 mult=1 m=1
XR12 net10 net9 VGND sky130_fd_pr__res_xhigh_po_2p85 L=31.52 mult=1 m=1
XR13 VGND net10 VGND sky130_fd_pr__res_xhigh_po_2p85 L=21.5 mult=1 m=1
XR17 net11 vbg VGND sky130_fd_pr__res_xhigh_po_2p85 L=31.52 mult=1 m=1
XR18 net12 net11 VGND sky130_fd_pr__res_xhigh_po_2p85 L=31.52 mult=1 m=1
XR19 net13 net12 VGND sky130_fd_pr__res_xhigh_po_2p85 L=31.52 mult=1 m=1
XR20 net14 net13 VGND sky130_fd_pr__res_xhigh_po_2p85 L=31.52 mult=1 m=1
XR21 VGND net14 VGND sky130_fd_pr__res_xhigh_po_2p85 L=16.62 mult=1 m=1
XR14 VGND VGND VGND sky130_fd_pr__res_xhigh_po_2p85 L=31.52 mult=2 m=2
XR15 VGND VGND VGND sky130_fd_pr__res_xhigh_po_2p85 L=21.5 mult=2 m=2
XR16 VGND VGND VGND sky130_fd_pr__res_xhigh_po_2p85 L=16.62 mult=2 m=2
XM11 Vx VGND VGND VGND sky130_fd_pr__nfet_01v8_lvt L=2 W=2 nf=1 ad='int((nf+1)/2) * W/nf * 0.29' as='int((nf+2)/2) * W/nf * 0.29'
+ pd='2*int((nf+1)/2) * (W/nf + 0.29)' ps='2*int((nf+2)/2) * (W/nf + 0.29)' nrd='0.29 / W' nrs='0.29 / W'
+ sa=0 sb=0 sd=0 mult=1 m=1
XM12 Vx VGND VGND VGND sky130_fd_pr__nfet_01v8_lvt L=2 W=2 nf=1 ad='int((nf+1)/2) * W/nf * 0.29' as='int((nf+2)/2) * W/nf * 0.29'
+ pd='2*int((nf+1)/2) * (W/nf + 0.29)' ps='2*int((nf+2)/2) * (W/nf + 0.29)' nrd='0.29 / W' nrs='0.29 / W'
+ sa=0 sb=0 sd=0 mult=1 m=1
XM14 VPWR VPWR VPWR VPWR sky130_fd_pr__pfet_01v8_lvt L=2 W=12.9 nf=1 ad='int((nf+1)/2) * W/nf * 0.29'
+ as='int((nf+2)/2) * W/nf * 0.29' pd='2*int((nf+1)/2) * (W/nf + 0.29)' ps='2*int((nf+2)/2) * (W/nf + 0.29)'
+ nrd='0.29 / W' nrs='0.29 / W' sa=0 sb=0 sd=0 mult=2 m=2
XM16 VGND VGND VGND VGND sky130_fd_pr__nfet_01v8_lvt L='2' W='9' nf=1 ad='int((nf+1)/2) * W/nf * 0.29'
+ as='int((nf+2)/2) * W/nf * 0.29' pd='2*int((nf+1)/2) * (W/nf + 0.29)' ps='2*int((nf+2)/2) * (W/nf + 0.29)'
+ nrd='0.29 / W' nrs='0.29 / W' sa=0 sb=0 sd=0 mult=2 m=2
XM17 Va VPWR VPWR VPWR sky130_fd_pr__pfet_01v8_lvt L=2 W=38.7 nf=1 ad='int((nf+1)/2) * W/nf * 0.29' as='int((nf+2)/2) * W/nf * 0.29'
+ pd='2*int((nf+1)/2) * (W/nf + 0.29)' ps='2*int((nf+2)/2) * (W/nf + 0.29)' nrd='0.29 / W' nrs='0.29 / W'
+ sa=0 sb=0 sd=0 mult=2 m=2
XC1 vgate VPWR sky130_fd_pr__cap_mim_m3_1 W=2 L=2 MF=100 m=100
XC2 Va VGND sky130_fd_pr__cap_mim_m3_2 W=2 L=2 MF=100 m=100
XQ1 VGND VGND Va sky130_fd_pr__pnp_05v5_W3p40L3p40 m=1
XQ2 VGND VGND vdm sky130_fd_pr__pnp_05v5_W3p40L3p40 m=1
XQ3 VGND VGND vdm sky130_fd_pr__pnp_05v5_W3p40L3p40 m=1
XQ4 VGND VGND vdm sky130_fd_pr__pnp_05v5_W3p40L3p40 m=1
XQ5 VGND VGND vdm sky130_fd_pr__pnp_05v5_W3p40L3p40 m=1
XQ6 VGND VGND vdm sky130_fd_pr__pnp_05v5_W3p40L3p40 m=1
XQ7 VGND VGND vdm sky130_fd_pr__pnp_05v5_W3p40L3p40 m=1
XQ8 VGND VGND vdm sky130_fd_pr__pnp_05v5_W3p40L3p40 m=1
XQ9 VGND VGND vdm sky130_fd_pr__pnp_05v5_W3p40L3p40 m=1
XQ10 VGND VGND vdm sky130_fd_pr__pnp_05v5_W3p40L3p40 m=1
XQ11 VGND VGND vdm sky130_fd_pr__pnp_05v5_W3p40L3p40 m=1
XQ12 VGND VGND vdm sky130_fd_pr__pnp_05v5_W3p40L3p40 m=1
XQ14 VGND VGND vdm sky130_fd_pr__pnp_05v5_W3p40L3p40 m=1
XQ15 VGND VGND vdm sky130_fd_pr__pnp_05v5_W3p40L3p40 m=1
XQ16 VGND VGND vdm sky130_fd_pr__pnp_05v5_W3p40L3p40 m=1
XQ17 VGND VGND vdm sky130_fd_pr__pnp_05v5_W3p40L3p40 m=1
XQ18 VGND VGND vdm sky130_fd_pr__pnp_05v5_W3p40L3p40 m=1
XQ19 VGND VGND vdm sky130_fd_pr__pnp_05v5_W3p40L3p40 m=1
XQ20 VGND VGND vdm sky130_fd_pr__pnp_05v5_W3p40L3p40 m=1
XQ21 VGND VGND vdm sky130_fd_pr__pnp_05v5_W3p40L3p40 m=1
XQ22 VGND VGND vdm sky130_fd_pr__pnp_05v5_W3p40L3p40 m=1
XQ23 VGND VGND vdm sky130_fd_pr__pnp_05v5_W3p40L3p40 m=1
XQ24 VGND VGND vdm sky130_fd_pr__pnp_05v5_W3p40L3p40 m=1
XQ25 VGND VGND vdm sky130_fd_pr__pnp_05v5_W3p40L3p40 m=1
XQ26 VGND VGND vdm sky130_fd_pr__pnp_05v5_W3p40L3p40 m=1
XQ27 VGND VGND vdm sky130_fd_pr__pnp_05v5_W3p40L3p40 m=1
XQ28 VGND VGND vdm sky130_fd_pr__pnp_05v5_W3p40L3p40 m=1
XQ29 VGND VGND vdm sky130_fd_pr__pnp_05v5_W3p40L3p40 m=1
XQ30 VGND VGND vdm sky130_fd_pr__pnp_05v5_W3p40L3p40 m=1
XQ31 VGND VGND vdm sky130_fd_pr__pnp_05v5_W3p40L3p40 m=1
XQ35 VGND VGND vdm sky130_fd_pr__pnp_05v5_W3p40L3p40 m=1
XQ36 VGND VGND vdm sky130_fd_pr__pnp_05v5_W3p40L3p40 m=1
XQ37 VGND VGND vdm sky130_fd_pr__pnp_05v5_W3p40L3p40 m=1
XQ38 VGND VGND vdm sky130_fd_pr__pnp_05v5_W3p40L3p40 m=1
XQ39 VGND VGND vdm sky130_fd_pr__pnp_05v5_W3p40L3p40 m=1
XQ40 VGND VGND vdm sky130_fd_pr__pnp_05v5_W3p40L3p40 m=1
XQ41 VGND VGND vdm sky130_fd_pr__pnp_05v5_W3p40L3p40 m=1
XQ42 VGND VGND vdm sky130_fd_pr__pnp_05v5_W3p40L3p40 m=1
XQ43 VGND VGND vdm sky130_fd_pr__pnp_05v5_W3p40L3p40 m=1
XQ44 VGND VGND vdm sky130_fd_pr__pnp_05v5_W3p40L3p40 m=1
.ends


* expanding   symbol:  analog_stdcells/skywater_asc_res_xhigh_po_2p85_1.sym # of pins=5
** sym_path: xschem/xschem/analog_stdcells/skywater_asc_res_xhigh_po_2p85_1.sym
** sch_path: xschem/xschem/analog_stdcells/skywater_asc_res_xhigh_po_2p85_1.sch
.subckt skywater_asc_res_xhigh_po_2p85_1 Rout Rin VPWR VGND VSUBS
*.iopin Rin
*.iopin Rout
*.iopin VPWR
*.iopin VGND
*.iopin VSUBS
XR1 net1 Rin VGND sky130_fd_pr__res_xhigh_po W=2.85 L=7.88 mult=1 m=1
XR2 net1 Rout VGND sky130_fd_pr__res_xhigh_po W=2.85 L=7.88 mult=1 m=1
.ends


* expanding   symbol:  xschem/skywater_asc_res_xhigh_po_2p85_2.sym # of pins=5
** sym_path: xschem/xschem/analog_stdcells/skywater_asc_res_xhigh_po_2p85_2.sym
** sch_path: xschem/xschem/analog_stdcells/skywater_asc_res_xhigh_po_2p85_2.sch
.subckt skywater_asc_res_xhigh_po_2p85_2 Rout Rin VPWR VSUB VGND
*.iopin Rin
*.iopin Rout
*.iopin VPWR
*.iopin VSUB
*.iopin VGND
XR1 net1 Rin VSUB sky130_fd_pr__res_xhigh_po W=2.85 L=10.75 mult=1 m=1
XR2 net1 Rout VSUB sky130_fd_pr__res_xhigh_po W=2.85 L=10.75 mult=1 m=1
.ends


* expanding   symbol:  xschem/sky130_asc_pnp_05v5_W3p40L3p40_8.sym # of pins=6
** sym_path: xschem/xschem/analog_stdcells/sky130_asc_pnp_05v5_W3p40L3p40_8.sym
** sch_path: xschem/xschem/analog_stdcells/sky130_asc_pnp_05v5_W3p40L3p40_8.sch
.subckt sky130_asc_pnp_05v5_W3p40L3p40_8 VPWR VGND VSUB Base Emitter Collector
*.iopin Base
*.iopin Emitter
*.iopin Collector
*.iopin VPWR
*.iopin VGND
*.iopin VSUB
XQ1 Collector Base Emitter sky130_fd_pr__pnp_05v5_W3p40L3p40 m=1
XQ2 Collector Base Emitter sky130_fd_pr__pnp_05v5_W3p40L3p40 m=1
XQ3 Collector Base Emitter sky130_fd_pr__pnp_05v5_W3p40L3p40 m=1
XQ4 Collector Base Emitter sky130_fd_pr__pnp_05v5_W3p40L3p40 m=1
XQ5 Collector Base Emitter sky130_fd_pr__pnp_05v5_W3p40L3p40 m=1
XQ6 Collector Base Emitter sky130_fd_pr__pnp_05v5_W3p40L3p40 m=1
XQ7 Collector Base Emitter sky130_fd_pr__pnp_05v5_W3p40L3p40 m=1
XQ8 Collector Base Emitter sky130_fd_pr__pnp_05v5_W3p40L3p40 m=1
.ends


* expanding   symbol:  xschem/sky130_asc_pnp_05v5_W3p40L3p40_7.sym # of pins=6
** sym_path: xschem/xschem/sky130_asc_pnp_05v5_W3p40L3p40_7.sym
** sch_path: xschem/xschem/sky130_asc_pnp_05v5_W3p40L3p40_7.sch
.subckt sky130_asc_pnp_05v5_W3p40L3p40_7 VPWR VGND VSUBS Base Emitter Collector
*.iopin Base
*.iopin Emitter
*.iopin Collector
*.iopin VPWR
*.iopin VGND
*.iopin VSUBS
XQ1 Collector Base Emitter sky130_fd_pr__pnp_05v5_W3p40L3p40 m=1
XQ2 Collector Base Emitter sky130_fd_pr__pnp_05v5_W3p40L3p40 m=1
XQ3 Collector Base Emitter sky130_fd_pr__pnp_05v5_W3p40L3p40 m=1
XQ4 Collector Base Emitter sky130_fd_pr__pnp_05v5_W3p40L3p40 m=1
XQ5 Collector Base Emitter sky130_fd_pr__pnp_05v5_W3p40L3p40 m=1
XQ6 Collector Base Emitter sky130_fd_pr__pnp_05v5_W3p40L3p40 m=1
XQ8 Collector Base Emitter sky130_fd_pr__pnp_05v5_W3p40L3p40 m=1
.ends


* expanding   symbol:  xschem/sky130_asc_pnp_05v5_W3p40L3p40_1.sym # of pins=5
** sym_path: xschem/xschem/sky130_asc_pnp_05v5_W3p40L3p40_1.sym
** sch_path: xschem/xschem/sky130_asc_pnp_05v5_W3p40L3p40_1.sch
.subckt sky130_asc_pnp_05v5_W3p40L3p40_1 VPWR VGND Base Collector Emitter
*.iopin Base
*.iopin Emitter
*.iopin Collector
*.iopin VPWR
*.iopin VGND
XQ1 Collector Base Emitter sky130_fd_pr__pnp_05v5_W3p40L3p40 m=1
.ends

.end
